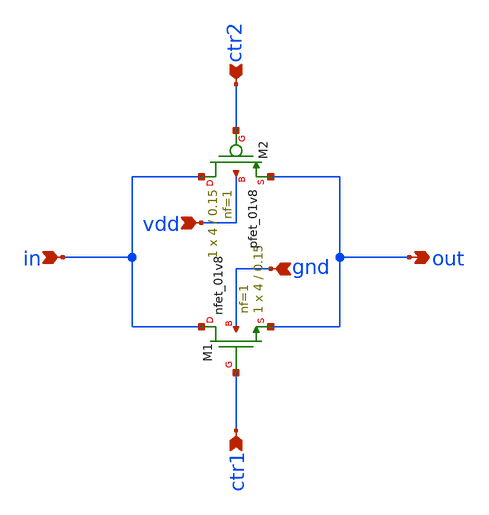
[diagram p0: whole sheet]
** sch_path: xschem/attenuator/transgate.sch
**.subckt transgate in ctr2 ctr1 vdd gnd out
*.ipin in
*.ipin ctr2
*.ipin ctr1
*.ipin vdd
*.ipin gnd
*.opin out
XM1 in ctr1 out gnd sky130_fd_pr__nfet_01v8 L=0.15 W=4 nf=1 ad='int((nf+1)/2) * W/nf * 0.29' as='int((nf+2)/2) * W/nf * 0.29'
+ pd='2*int((nf+1)/2) * (W/nf + 0.29)' ps='2*int((nf+2)/2) * (W/nf + 0.29)' nrd='0.29 / W' nrs='0.29 / W'
+ sa=0 sb=0 sd=0 mult=1 m=1
XM2 in ctr2 out vdd sky130_fd_pr__pfet_01v8 L=0.15 W=4 nf=1 ad='int((nf+1)/2) * W/nf * 0.29' as='int((nf+2)/2) * W/nf * 0.29'
+ pd='2*int((nf+1)/2) * (W/nf + 0.29)' ps='2*int((nf+2)/2) * (W/nf + 0.29)' nrd='0.29 / W' nrs='0.29 / W'
+ sa=0 sb=0 sd=0 mult=1 m=1
**.ends
.end
